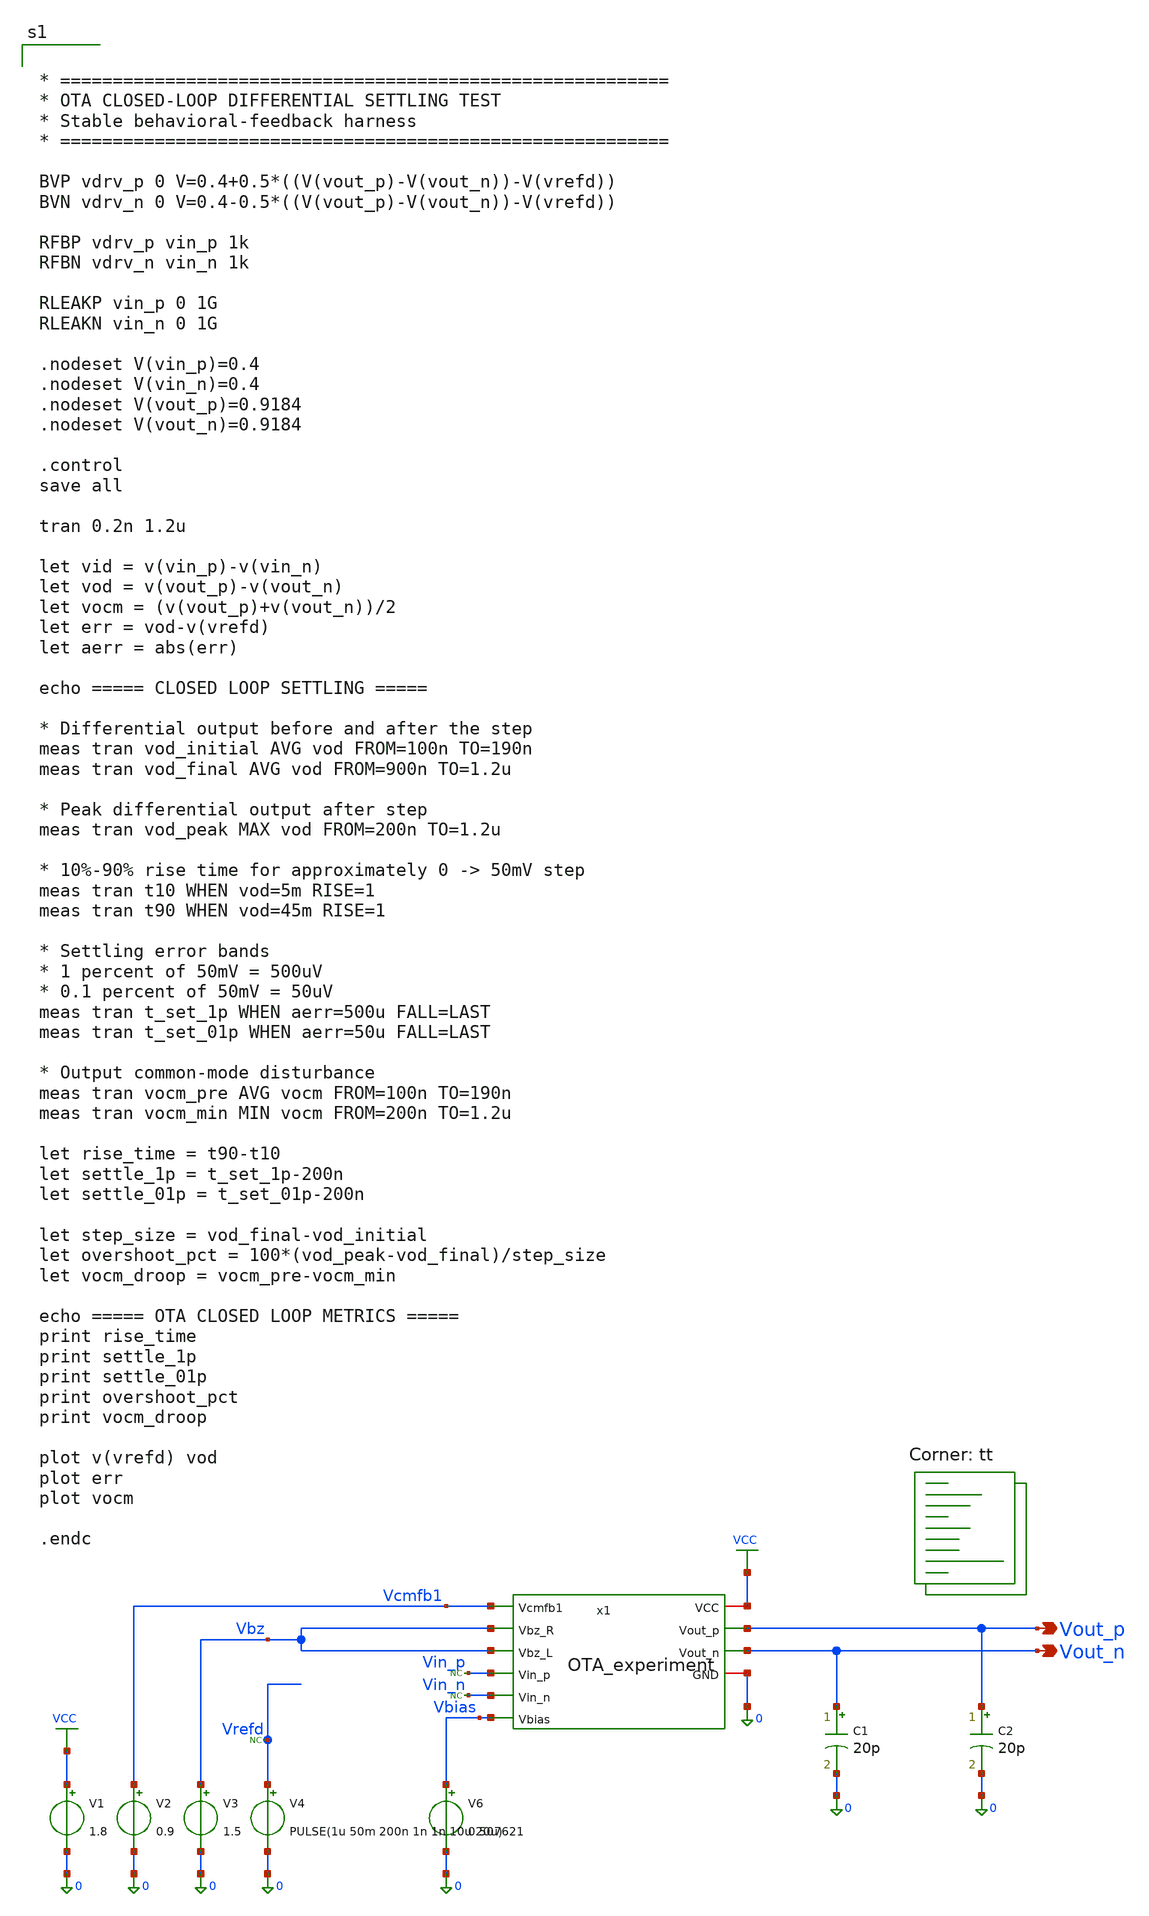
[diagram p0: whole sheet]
** sch_path: blocks/01_OTA/sim/tb_OTA_Tran_CL_experiment.sch
**.subckt tb_OTA_Tran_CL_experiment Vout_p Vout_n
*.opin Vout_p
*.opin Vout_n
V1 VCC 0 1.8
V2 Vcmfb1 0 0.9
V3 Vbz 0 1.5
V4 Vrefd 0 PULSE(1u 50m 200n 1n 1n 10u 20u)
V6 Vbias 0 0.507621
C1 Vout_n 0 20p m=1
C2 Vout_p 0 20p m=1
* noconn Vrefd
* noconn Vin_p
* noconn Vin_n
x1 VCC Vcmfb1 Vbz Vbz Vin_p Vin_n Vout_p Vout_n Vbias 0 OTA_experiment
**** begin user architecture code


* ==========================================================
* OTA CLOSED-LOOP DIFFERENTIAL SETTLING TEST
* Stable behavioral-feedback harness
* ==========================================================

BVP vdrv_p 0 V=0.4+0.5*((V(vout_p)-V(vout_n))-V(vrefd))
BVN vdrv_n 0 V=0.4-0.5*((V(vout_p)-V(vout_n))-V(vrefd))

RFBP vdrv_p vin_p 1k
RFBN vdrv_n vin_n 1k

RLEAKP vin_p 0 1G
RLEAKN vin_n 0 1G

.nodeset V(vin_p)=0.4
.nodeset V(vin_n)=0.4
.nodeset V(vout_p)=0.9184
.nodeset V(vout_n)=0.9184

.control
save all

tran 0.2n 1.2u

let vid = v(vin_p)-v(vin_n)
let vod = v(vout_p)-v(vout_n)
let vocm = (v(vout_p)+v(vout_n))/2
let err = vod-v(vrefd)
let aerr = abs(err)

echo ===== CLOSED LOOP SETTLING =====

* Differential output before and after the step
meas tran vod_initial AVG vod FROM=100n TO=190n
meas tran vod_final AVG vod FROM=900n TO=1.2u

* Peak differential output after step
meas tran vod_peak MAX vod FROM=200n TO=1.2u

* 10%-90% rise time for approximately 0 -> 50mV step
meas tran t10 WHEN vod=5m RISE=1
meas tran t90 WHEN vod=45m RISE=1

* Settling error bands
* 1 percent of 50mV = 500uV
* 0.1 percent of 50mV = 50uV
meas tran t_set_1p WHEN aerr=500u FALL=LAST
meas tran t_set_01p WHEN aerr=50u FALL=LAST

* Output common-mode disturbance
meas tran vocm_pre AVG vocm FROM=100n TO=190n
meas tran vocm_min MIN vocm FROM=200n TO=1.2u

let rise_time = t90-t10
let settle_1p = t_set_1p-200n
let settle_01p = t_set_01p-200n

let step_size = vod_final-vod_initial
let overshoot_pct = 100*(vod_peak-vod_final)/step_size
let vocm_droop = vocm_pre-vocm_min

echo ===== OTA CLOSED LOOP METRICS =====
print rise_time
print settle_1p
print settle_01p
print overshoot_pct
print vocm_droop

plot v(vrefd) vod
plot err
plot vocm

.endc


.lib $::SKYWATER_MODELS/sky130.lib.spice tt
**** end user architecture code
**.ends

* expanding   symbol:  blocks/01_OTA/xschem/OTA_experiment.sym # of pins=10
** sym_path: blocks/01_OTA/xschem/OTA_experiment.sym
** sch_path: blocks/01_OTA/xschem/OTA_experiment.sch
.subckt OTA_experiment VCC Vcmfb1 Vbz_R Vbz_L Vin_p Vin_n Vout_p Vout_n Vbias GND
*.ipin Vin_p
*.ipin Vin_n
*.ipin Vbias
*.ipin Vbz_R
*.ipin Vbz_L
*.ipin Vcmfb1
*.opin Vout_p
*.opin Vout_n
*.iopin VCC
*.iopin GND
XM1 net5 Vin_p net3 net5 sky130_fd_pr__pfet_01v8 L=1.2 W=120 nf=1 ad='int((1 + 1)/2) * 120 / 1 * 0.29'
+ as='int((1 + 2)/2) * 120 / 1 * 0.29' pd='2*int((1 + 1)/2) * (120 / 1 + 0.29)' ps='2*int((1 + 2)/2) * (120 / 1 + 0.29)'
+ nrd='0.29 / 120 ' nrs='0.29 / 120 ' sa=0 sb=0 sd=0 mult=1 m=1
XM2 net5 Vin_n net4 net5 sky130_fd_pr__pfet_01v8 L=1.2 W=120 nf=1 ad='int((1 + 1)/2) * 120 / 1 * 0.29'
+ as='int((1 + 2)/2) * 120 / 1 * 0.29' pd='2*int((1 + 1)/2) * (120 / 1 + 0.29)' ps='2*int((1 + 2)/2) * (120 / 1 + 0.29)'
+ nrd='0.29 / 120 ' nrs='0.29 / 120 ' sa=0 sb=0 sd=0 mult=1 m=1
XM3 net3 Vbias GND GND sky130_fd_pr__nfet_01v8 L=2 W=8 nf=1 ad='int((1 + 1)/2) * 8 / 1 * 0.29' as='int((1 + 2)/2) * 8 / 1 * 0.29'
+ pd='2*int((1 + 1)/2) * (8 / 1 + 0.29)' ps='2*int((1 + 2)/2) * (8 / 1 + 0.29)' nrd='0.29 / 8 ' nrs='0.29 / 8 '
+ sa=0 sb=0 sd=0 mult=1 m=1
XM4 net4 Vbias GND GND sky130_fd_pr__nfet_01v8 L=2 W=8 nf=1 ad='int((1 + 1)/2) * 8 / 1 * 0.29' as='int((1 + 2)/2) * 8 / 1 * 0.29'
+ pd='2*int((1 + 1)/2) * (8 / 1 + 0.29)' ps='2*int((1 + 2)/2) * (8 / 1 + 0.29)' nrd='0.29 / 8 ' nrs='0.29 / 8 '
+ sa=0 sb=0 sd=0 mult=1 m=1
XM5 net1 net4 GND GND sky130_fd_pr__nfet_01v8 L=2 W=20 nf=1 ad='int((1 + 1)/2) * 20 / 1 * 0.29' as='int((1 + 2)/2) * 20 / 1 * 0.29'
+ pd='2*int((1 + 1)/2) * (20 / 1 + 0.29)' ps='2*int((1 + 2)/2) * (20 / 1 + 0.29)' nrd='0.29 / 20 ' nrs='0.29 / 20 '
+ sa=0 sb=0 sd=0 mult=1 m=1
XM6 net2 net3 GND GND sky130_fd_pr__nfet_01v8 L=2 W=20 nf=1 ad='int((1 + 1)/2) * 20 / 1 * 0.29' as='int((1 + 2)/2) * 20 / 1 * 0.29'
+ pd='2*int((1 + 1)/2) * (20 / 1 + 0.29)' ps='2*int((1 + 2)/2) * (20 / 1 + 0.29)' nrd='0.29 / 20 ' nrs='0.29 / 20 '
+ sa=0 sb=0 sd=0 mult=1 m=1
XM7 VCC net1 net1 VCC sky130_fd_pr__pfet_01v8 L=2 W=30 nf=1 ad='int((1 + 1)/2) * 30 / 1 * 0.29' as='int((1 + 2)/2) * 30 / 1 * 0.29'
+ pd='2*int((1 + 1)/2) * (30 / 1 + 0.29)' ps='2*int((1 + 2)/2) * (30 / 1 + 0.29)' nrd='0.29 / 30 ' nrs='0.29 / 30 '
+ sa=0 sb=0 sd=0 mult=1 m=1
XM8 VCC net2 net2 VCC sky130_fd_pr__pfet_01v8 L=2 W=30 nf=1 ad='int((1 + 1)/2) * 30 / 1 * 0.29' as='int((1 + 2)/2) * 30 / 1 * 0.29'
+ pd='2*int((1 + 1)/2) * (30 / 1 + 0.29)' ps='2*int((1 + 2)/2) * (30 / 1 + 0.29)' nrd='0.29 / 30 ' nrs='0.29 / 30 '
+ sa=0 sb=0 sd=0 mult=1 m=1
XM9 VCC net1 Vout_p VCC sky130_fd_pr__pfet_01v8 L=1 W=300 nf=1 ad='int((1 + 1)/2) * 300 / 1 * 0.29' as='int((1 + 2)/2) * 300 / 1 * 0.29'
+ pd='2*int((1 + 1)/2) * (300 / 1 + 0.29)' ps='2*int((1 + 2)/2) * (300 / 1 + 0.29)' nrd='0.29 / 300 ' nrs='0.29 / 300 '
+ sa=0 sb=0 sd=0 mult=1 m=1
XM10 VCC net2 Vout_n VCC sky130_fd_pr__pfet_01v8 L=1 W=300 nf=1 ad='int((1 + 1)/2) * 300 / 1 * 0.29'
+ as='int((1 + 2)/2) * 300 / 1 * 0.29' pd='2*int((1 + 1)/2) * (300 / 1 + 0.29)' ps='2*int((1 + 2)/2) * (300 / 1 + 0.29)'
+ nrd='0.29 / 300 ' nrs='0.29 / 300 ' sa=0 sb=0 sd=0 mult=1 m=1
XM11 Vout_p net4 GND GND sky130_fd_pr__nfet_01v8 L=1 W=200 nf=1 ad='int((1 + 1)/2) * 200 / 1 * 0.29'
+ as='int((1 + 2)/2) * 200 / 1 * 0.29' pd='2*int((1 + 1)/2) * (200 / 1 + 0.29)' ps='2*int((1 + 2)/2) * (200 / 1 + 0.29)'
+ nrd='0.29 / 200 ' nrs='0.29 / 200 ' sa=0 sb=0 sd=0 mult=1 m=1
XM12 Vout_n net3 GND GND sky130_fd_pr__nfet_01v8 L=1 W=200 nf=1 ad='int((1 + 1)/2) * 200 / 1 * 0.29'
+ as='int((1 + 2)/2) * 200 / 1 * 0.29' pd='2*int((1 + 1)/2) * (200 / 1 + 0.29)' ps='2*int((1 + 2)/2) * (200 / 1 + 0.29)'
+ nrd='0.29 / 200 ' nrs='0.29 / 200 ' sa=0 sb=0 sd=0 mult=1 m=1
XM13 VCC Vcmfb1 net5 VCC sky130_fd_pr__pfet_01v8 L=1.2 W=60 nf=1 ad='int((1 + 1)/2) * 60 / 1 * 0.29'
+ as='int((1 + 2)/2) * 60 / 1 * 0.29' pd='2*int((1 + 1)/2) * (60 / 1 + 0.29)' ps='2*int((1 + 2)/2) * (60 / 1 + 0.29)'
+ nrd='0.29 / 60 ' nrs='0.29 / 60 ' sa=0 sb=0 sd=0 mult=1 m=1
XC1 Vout_p net4 sky130_fd_pr__cap_mim_m3_1 W=1 L=1 MF=80 m=80
XC2 net3 Vout_n sky130_fd_pr__cap_mim_m3_1 W=1 L=1 MF=80 m=80
.ends

.GLOBAL VCC
.end
